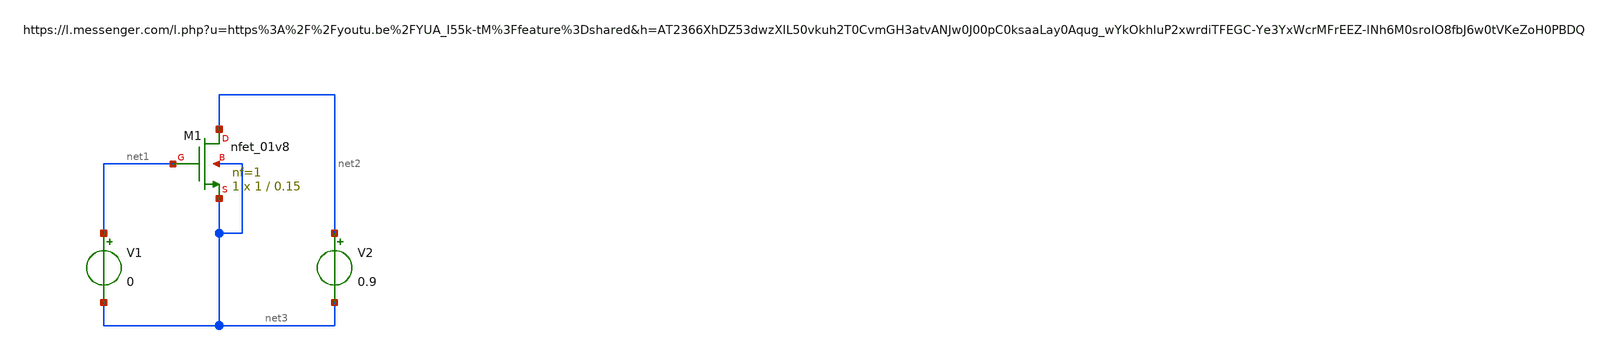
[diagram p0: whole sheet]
** sch_path: pre_layout_sim/nfet_characterization/nfet_characterization.sch
**.subckt nfet_characterization
XM1 net2 net1 net3 net3 sky130_fd_pr__nfet_01v8 L=0.15 W=1 nf=1 ad='int((1 + 1)/2) * 1 / 1 * 0.29' as='int((1 + 2)/2) * 1 / 1 * 0.29'
+ pd='2*int((1 + 1)/2) * (1 / 1 + 0.29)' ps='2*int((1 + 2)/2) * (1 / 1 + 0.29)' nrd='0.29 / 1 ' nrs='0.29 / 1 '
+ sa=0 sb=0 sd=0 mult=1 m=1
V1 net1 net3 0
V2 net2 net3 0.9
**** begin user architecture code


.control
save all @m.xm1.msky130_fd_pr__nfet_01v8[id]
dc V1 0 3 0.01
write nfet_characterization.raw
.endc



** opencircuitdesign pdks install
.lib $::SKYWATER_MODELS/sky130.lib.spice tt

**** end user architecture code
**.ends
.end
